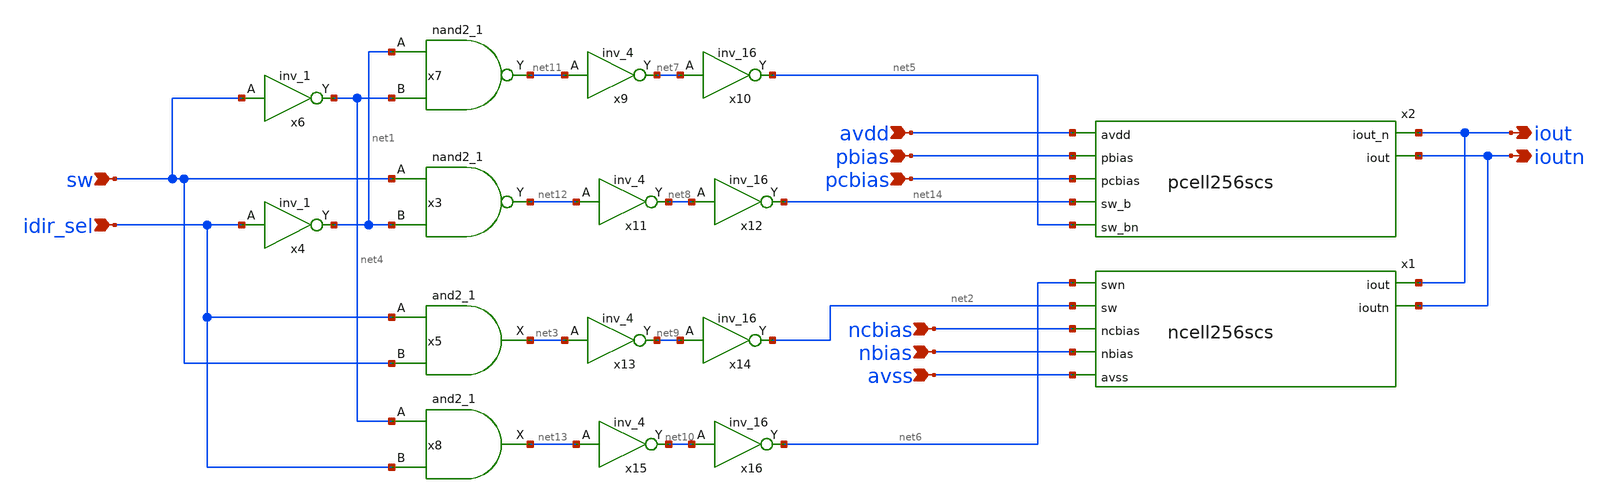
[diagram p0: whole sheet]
** sch_path: xschem/icell256_unary_scs.sch
**.subckt icell256_unary_scs avdd pbias pcbias sw idir_sel ncbias nbias avss iout ioutn
*.ipin avdd
*.ipin pbias
*.ipin pcbias
*.ipin sw
*.ipin idir_sel
*.ipin ncbias
*.ipin nbias
*.ipin avss
*.opin iout
*.opin ioutn
x3 sw net1 avss avss avdd avdd net12 sky130_fd_sc_hvl__nand2_1
x5 idir_sel sw avss avss avdd avdd net3 sky130_fd_sc_hvl__and2_1
x4 idir_sel avss avss avdd avdd net1 sky130_fd_sc_hvl__inv_1
x6 sw avss avss avdd avdd net4 sky130_fd_sc_hvl__inv_1
x7 net1 net4 avss avss avdd avdd net11 sky130_fd_sc_hvl__nand2_1
x8 net4 idir_sel avss avss avdd avdd net13 sky130_fd_sc_hvl__and2_1
x1 iout ioutn net6 net2 ncbias nbias avss ncell256scs
x2 avdd pbias pcbias net14 net5 iout ioutn pcell256scs
x9 net11 avss avss avdd avdd net7 sky130_fd_sc_hvl__inv_4
x10 net7 avss avss avdd avdd net5 sky130_fd_sc_hvl__inv_16
x11 net12 avss avss avdd avdd net8 sky130_fd_sc_hvl__inv_4
x12 net8 avss avss avdd avdd net14 sky130_fd_sc_hvl__inv_16
x13 net3 avss avss avdd avdd net9 sky130_fd_sc_hvl__inv_4
x14 net9 avss avss avdd avdd net2 sky130_fd_sc_hvl__inv_16
x15 net13 avss avss avdd avdd net10 sky130_fd_sc_hvl__inv_4
x16 net10 avss avss avdd avdd net6 sky130_fd_sc_hvl__inv_16
**.ends

* expanding   symbol:  ncell256scs.sym # of pins=7
** sym_path: xschem/ncell256scs.sym
** sch_path: xschem/ncell256scs.sch
.subckt ncell256scs iout ioutn swn sw ncbias nbias avss
*.ipin sw
*.ipin ncbias
*.ipin nbias
*.ipin avss
*.opin iout
*.opin ioutn
*.ipin swn
XM8 net1 nbias avss avss sky130_fd_pr__nfet_g5v0d10v5 L=1 W=3 nf=1 ad='int((nf+1)/2) * W/nf * 0.29' as='int((nf+2)/2) * W/nf * 0.29'
+ pd='2*int((nf+1)/2) * (W/nf + 0.29)' ps='2*int((nf+2)/2) * (W/nf + 0.29)' nrd='0.29 / W' nrs='0.29 / W'
+ sa=0 sb=0 sd=0 mult=256 m=256
XM9 net2 ncbias net1 avss sky130_fd_pr__nfet_g5v0d10v5 L=1 W=6 nf=1 ad='int((nf+1)/2) * W/nf * 0.29'
+ as='int((nf+2)/2) * W/nf * 0.29' pd='2*int((nf+1)/2) * (W/nf + 0.29)' ps='2*int((nf+2)/2) * (W/nf + 0.29)'
+ nrd='0.29 / W' nrs='0.29 / W' sa=0 sb=0 sd=0 mult=256 m=256
XM1 iout sw net2 avss sky130_fd_pr__nfet_g5v0d10v5 L=1 W=6 nf=1 ad='int((nf+1)/2) * W/nf * 0.29' as='int((nf+2)/2) * W/nf * 0.29'
+ pd='2*int((nf+1)/2) * (W/nf + 0.29)' ps='2*int((nf+2)/2) * (W/nf + 0.29)' nrd='0.29 / W' nrs='0.29 / W'
+ sa=0 sb=0 sd=0 mult=256 m=256
XM2 ioutn swn net2 avss sky130_fd_pr__nfet_g5v0d10v5 L=1 W=6 nf=1 ad='int((nf+1)/2) * W/nf * 0.29' as='int((nf+2)/2) * W/nf * 0.29'
+ pd='2*int((nf+1)/2) * (W/nf + 0.29)' ps='2*int((nf+2)/2) * (W/nf + 0.29)' nrd='0.29 / W' nrs='0.29 / W'
+ sa=0 sb=0 sd=0 mult=256 m=256
.ends


* expanding   symbol:  pcell256scs.sym # of pins=7
** sym_path: xschem/pcell256scs.sym
** sch_path: xschem/pcell256scs.sch
.subckt pcell256scs avdd pbias pcbias sw_b sw_bn iout_n iout
*.ipin pbias
*.ipin pcbias
*.ipin sw_b
*.ipin avdd
*.opin iout
*.opin iout_n
*.ipin sw_bn
XM1 net1 pbias avdd avdd sky130_fd_pr__pfet_g5v0d10v5 L=1 W=6 nf=1 ad='int((nf+1)/2) * W/nf * 0.29' as='int((nf+2)/2) * W/nf * 0.29'
+ pd='2*int((nf+1)/2) * (W/nf + 0.29)' ps='2*int((nf+2)/2) * (W/nf + 0.29)' nrd='0.29 / W' nrs='0.29 / W'
+ sa=0 sb=0 sd=0 mult=256 m=256
XM2 net2 pcbias net1 avdd sky130_fd_pr__pfet_g5v0d10v5 L=1 W=12 nf=1 ad='int((nf+1)/2) * W/nf * 0.29'
+ as='int((nf+2)/2) * W/nf * 0.29' pd='2*int((nf+1)/2) * (W/nf + 0.29)' ps='2*int((nf+2)/2) * (W/nf + 0.29)'
+ nrd='0.29 / W' nrs='0.29 / W' sa=0 sb=0 sd=0 mult=256 m=256
XM3 iout sw_b net2 avdd sky130_fd_pr__pfet_g5v0d10v5 L=1 W=4 nf=1 ad='int((nf+1)/2) * W/nf * 0.29' as='int((nf+2)/2) * W/nf * 0.29'
+ pd='2*int((nf+1)/2) * (W/nf + 0.29)' ps='2*int((nf+2)/2) * (W/nf + 0.29)' nrd='0.29 / W' nrs='0.29 / W'
+ sa=0 sb=0 sd=0 mult=256 m=256
XM4 iout_n sw_bn net2 avdd sky130_fd_pr__pfet_g5v0d10v5 L=1 W=4 nf=1 ad='int((nf+1)/2) * W/nf * 0.29'
+ as='int((nf+2)/2) * W/nf * 0.29' pd='2*int((nf+1)/2) * (W/nf + 0.29)' ps='2*int((nf+2)/2) * (W/nf + 0.29)'
+ nrd='0.29 / W' nrs='0.29 / W' sa=0 sb=0 sd=0 mult=256 m=256
.ends

.end
